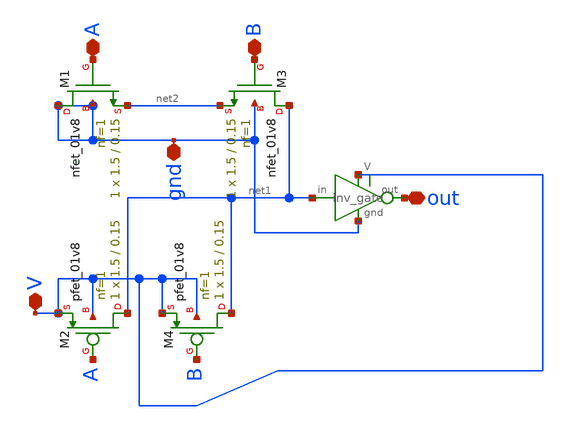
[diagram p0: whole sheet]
** sch_path: xschem/designs/counter4b/and_gate.sch
* xschem/designs/counter4b/inv_gate.sym:
* Copyright 2022 Stefan Frederik Schippers
* Licensed under the Apache License, Version 2.0 (the "License");
**.subckt and_gate A out gnd V B
*.iopin A
*.iopin out
*.iopin gnd
*.iopin V
*.iopin B
XM1 gnd A net2 gnd sky130_fd_pr__nfet_01v8 L=0.15 W=1.5 nf=1 ad='int((nf+1)/2) * W/nf * 0.29' as='int((nf+2)/2) * W/nf * 0.29'
+ pd='2*int((nf+1)/2) * (W/nf + 0.29)' ps='2*int((nf+2)/2) * (W/nf + 0.29)' nrd='0.29 / W' nrs='0.29 / W'
+ sa=0 sb=0 sd=0 mult=1 m=1
XM2 net1 A V V sky130_fd_pr__pfet_01v8 L=0.15 W=1.5 nf=1 ad='int((nf+1)/2) * W/nf * 0.29' as='int((nf+2)/2) * W/nf * 0.29'
+ pd='2*int((nf+1)/2) * (W/nf + 0.29)' ps='2*int((nf+2)/2) * (W/nf + 0.29)' nrd='0.29 / W' nrs='0.29 / W'
+ sa=0 sb=0 sd=0 mult=1 m=1
XM3 net1 B net2 gnd sky130_fd_pr__nfet_01v8 L=0.15 W=1.5 nf=1 ad='int((nf+1)/2) * W/nf * 0.29' as='int((nf+2)/2) * W/nf * 0.29'
+ pd='2*int((nf+1)/2) * (W/nf + 0.29)' ps='2*int((nf+2)/2) * (W/nf + 0.29)' nrd='0.29 / W' nrs='0.29 / W'
+ sa=0 sb=0 sd=0 mult=1 m=1
XM4 net1 B V V sky130_fd_pr__pfet_01v8 L=0.15 W=1.5 nf=1 ad='int((nf+1)/2) * W/nf * 0.29' as='int((nf+2)/2) * W/nf * 0.29'
+ pd='2*int((nf+1)/2) * (W/nf + 0.29)' ps='2*int((nf+2)/2) * (W/nf + 0.29)' nrd='0.29 / W' nrs='0.29 / W'
+ sa=0 sb=0 sd=0 mult=1 m=1
X1 V gnd net1 out inv_gate
**.ends

* expanding   symbol:  inv_gate.sym # of pins=4
** sym_path: xschem/designs/counter4b/inv_gate.sym
** sch_path: xschem/designs/counter4b/inv_gate.sch
.subckt inv_gate V gnd in out
*.iopin in
*.iopin out
*.iopin gnd
*.iopin V
XM1 out in gnd gnd sky130_fd_pr__nfet_01v8 L=0.15 W=0.75 nf=1 ad='int((nf+1)/2) * W/nf * 0.29' as='int((nf+2)/2) * W/nf * 0.29'
+ pd='2*int((nf+1)/2) * (W/nf + 0.29)' ps='2*int((nf+2)/2) * (W/nf + 0.29)' nrd='0.29 / W' nrs='0.29 / W'
+ sa=0 sb=0 sd=0 mult=1 m=1
XM2 out in V V sky130_fd_pr__pfet_01v8 L=0.15 W=1.5 nf=1 ad='int((nf+1)/2) * W/nf * 0.29' as='int((nf+2)/2) * W/nf * 0.29'
+ pd='2*int((nf+1)/2) * (W/nf + 0.29)' ps='2*int((nf+2)/2) * (W/nf + 0.29)' nrd='0.29 / W' nrs='0.29 / W'
+ sa=0 sb=0 sd=0 mult=1 m=1
.ends

.end
